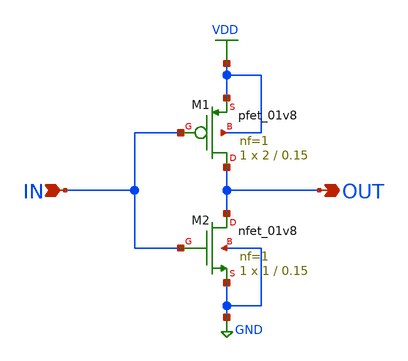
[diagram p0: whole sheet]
** sch_path: xschem/inverter.sch
**.subckt inverter IN OUT
*.ipin IN
*.opin OUT
XM1 OUT IN VDD VDD sky130_fd_pr__pfet_01v8 L=0.15 W=2 nf=1 ad=0.58 as=0.58 pd=4.58 ps=4.58 nrd=0.145
+ nrs=0.145 sa=0 sb=0 sd=0 mult=1 m=1
XM2 OUT IN GND GND sky130_fd_pr__nfet_01v8 L=0.15 W=1 nf=1 ad=0.29 as=0.29 pd=2.58 ps=2.58 nrd=0.29
+ nrs=0.29 sa=0 sb=0 sd=0 mult=1 m=1
**.ends
.GLOBAL VDD
.GLOBAL GND
.end
